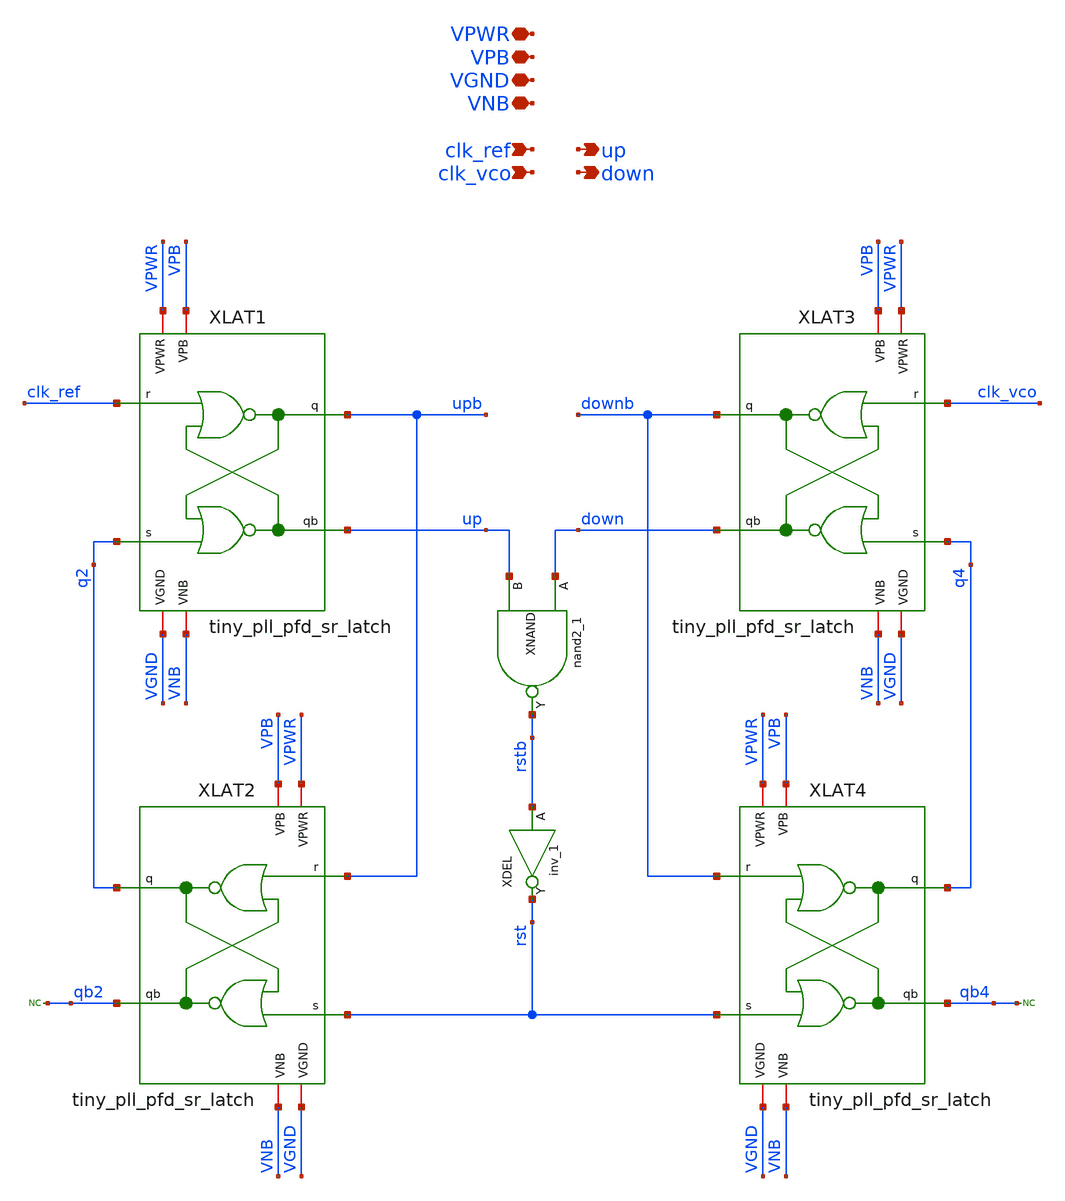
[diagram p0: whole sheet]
** sch_path: xschem/tiny_pll/tiny_pll_pfd.sch
**.subckt tiny_pll_pfd clk_ref clk_vco down VNB VGND VPB VPWR up
*.ipin clk_ref
*.ipin clk_vco
*.opin down
*.iopin VNB
*.iopin VGND
*.iopin VPB
*.iopin VPWR
*.opin up
XLAT1 VPWR VPB VGND VNB upb q2 up clk_ref tiny_pll_pfd_sr_latch
XLAT2 VPWR VPB VGND VNB q2 rst qb2 upb tiny_pll_pfd_sr_latch
* noconn qb2
XLAT3 VPWR VPB VGND VNB downb q4 down clk_vco tiny_pll_pfd_sr_latch
XLAT4 VPWR VPB VGND VNB q4 rst qb4 downb tiny_pll_pfd_sr_latch
* noconn qb4
XNAND down up VGND VNB VPB VPWR rstb sky130_fd_sc_hd__nand2_1
XDEL rstb VGND VNB VPB VPWR rst sky130_fd_sc_hd__inv_1
**.ends

* expanding   symbol:  tiny_pll_pfd_sr_latch.sym # of pins=8
** sym_path: xschem/tiny_pll/tiny_pll_pfd_sr_latch.sym
** sch_path: xschem/tiny_pll/tiny_pll_pfd_sr_latch.sch
.subckt tiny_pll_pfd_sr_latch VPWR VPB VGND VNB q s qb r
*.ipin s
*.ipin r
*.opin q
*.opin qb
*.iopin VNB
*.iopin VGND
*.iopin VPB
*.iopin VPWR
XR qb r VGND VNB VPB VPWR q sky130_fd_sc_hd__nor2_1
XS q s VGND VNB VPB VPWR qb sky130_fd_sc_hd__nor2_1
.ends

.end
